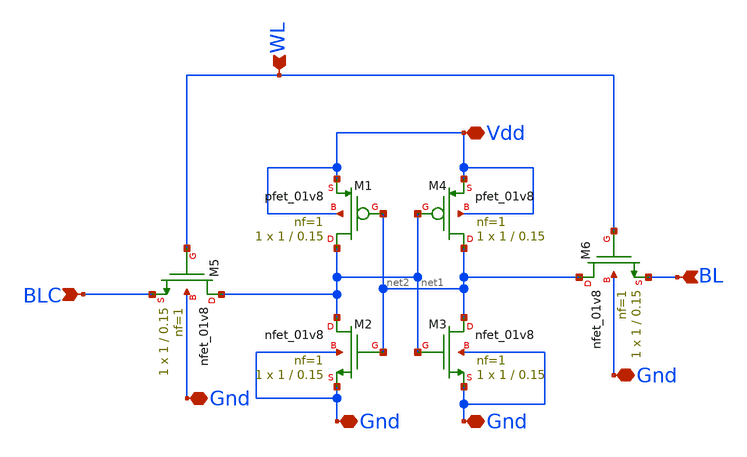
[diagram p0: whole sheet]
** sch_path: Schematic/SRam/SRam.sch
**.subckt SRam BL BLC Vdd WL Gnd Gnd Gnd Gnd
*.ipin BL
*.ipin BLC
*.iopin Vdd
*.ipin WL
*.iopin Gnd
*.iopin Gnd
*.iopin Gnd
*.iopin Gnd
XM2 net1 net2 Gnd Gnd sky130_fd_pr__nfet_01v8 L=0.15 W=1 nf=1 ad='int((1 + 1)/2) * 1 / 1 * 0.29' as='int((1 + 2)/2) * 1 / 1 * 0.29'
+ pd='2*int((1 + 1)/2) * (1 / 1 + 0.29)' ps='2*int((1 + 2)/2) * (1 / 1 + 0.29)' nrd='0.29 / 1 ' nrs='0.29 / 1 '
+ sa=0 sb=0 sd=0 mult=1 m=1
XM1 net1 net2 Vdd Vdd sky130_fd_pr__pfet_01v8 L=0.15 W=1 nf=1 ad='int((1 + 1)/2) * 1 / 1 * 0.29' as='int((1 + 2)/2) * 1 / 1 * 0.29'
+ pd='2*int((1 + 1)/2) * (1 / 1 + 0.29)' ps='2*int((1 + 2)/2) * (1 / 1 + 0.29)' nrd='0.29 / 1 ' nrs='0.29 / 1 '
+ sa=0 sb=0 sd=0 mult=1 m=1
XM3 net2 net1 Gnd Gnd sky130_fd_pr__nfet_01v8 L=0.15 W=1 nf=1 ad='int((1 + 1)/2) * 1 / 1 * 0.29' as='int((1 + 2)/2) * 1 / 1 * 0.29'
+ pd='2*int((1 + 1)/2) * (1 / 1 + 0.29)' ps='2*int((1 + 2)/2) * (1 / 1 + 0.29)' nrd='0.29 / 1 ' nrs='0.29 / 1 '
+ sa=0 sb=0 sd=0 mult=1 m=1
XM4 net2 net1 Vdd Vdd sky130_fd_pr__pfet_01v8 L=0.15 W=1 nf=1 ad='int((1 + 1)/2) * 1 / 1 * 0.29' as='int((1 + 2)/2) * 1 / 1 * 0.29'
+ pd='2*int((1 + 1)/2) * (1 / 1 + 0.29)' ps='2*int((1 + 2)/2) * (1 / 1 + 0.29)' nrd='0.29 / 1 ' nrs='0.29 / 1 '
+ sa=0 sb=0 sd=0 mult=1 m=1
XM6 net2 WL BL Gnd sky130_fd_pr__nfet_01v8 L=0.15 W=1 nf=1 ad='int((1 + 1)/2) * 1 / 1 * 0.29' as='int((1 + 2)/2) * 1 / 1 * 0.29'
+ pd='2*int((1 + 1)/2) * (1 / 1 + 0.29)' ps='2*int((1 + 2)/2) * (1 / 1 + 0.29)' nrd='0.29 / 1 ' nrs='0.29 / 1 '
+ sa=0 sb=0 sd=0 mult=1 m=1
XM5 net1 WL BLC Gnd sky130_fd_pr__nfet_01v8 L=0.15 W=1 nf=1 ad='int((1 + 1)/2) * 1 / 1 * 0.29' as='int((1 + 2)/2) * 1 / 1 * 0.29'
+ pd='2*int((1 + 1)/2) * (1 / 1 + 0.29)' ps='2*int((1 + 2)/2) * (1 / 1 + 0.29)' nrd='0.29 / 1 ' nrs='0.29 / 1 '
+ sa=0 sb=0 sd=0 mult=1 m=1
**.ends
.end
